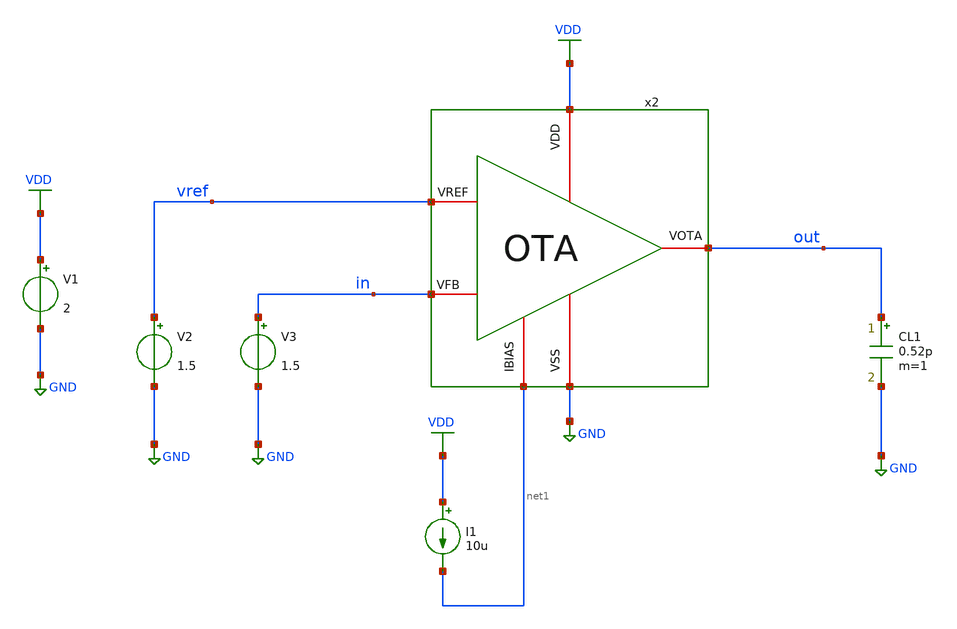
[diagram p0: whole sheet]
** sch_path: designs/libs/tb_ldo/tb_ldo/tb_ldo_OTA/tb_ldo_OTA_noise/tb_ldo_OTA_noise.sch
**.subckt tb_ldo_OTA_noise
V1 VDD GND 2
V2 vref GND 1.5
I1 VDD net1 10u
CL1 out GND 0.52p m=1
V3 in GND 1.5
x2 VDD vref in out net1 GND OTA
**** begin user architecture code



.control
save all

** Set sources
alter @V1[AC] = 1

** Simulation
op
noise v(out) V1 dec 100 1 10G

** Plots
setplot noise1
plot onoise_spectrum
plot inoise_spectrum

** Measurements
let output_noise_at_1MHz = onoise_spectrum[600]
print output_noise_at_1MHz

write tb_ldo_OTA_noise.raw

.endc
* ngspice commands




.include $::180MCU_MODELS/design.ngspice
.lib $::180MCU_MODELS/sm141064.ngspice typical
.lib $::180MCU_MODELS/sm141064.ngspice cap_mim
.lib $::180MCU_MODELS/sm141064.ngspice moscap_typical
.lib $::180MCU_MODELS/sm141064.ngspice mimcap_typical
.lib $::180MCU_MODELS/sm141064.ngspice res_typical
* .lib $::180MCU_MODELS/sm141064.ngspice res_statistical
* ngspice commands

**** end user architecture code
**.ends

* expanding   symbol:  libs/core_ldo/ldo/ldo_OTA/OTA.sym # of pins=6
** sym_path: designs/libs/core_ldo/ldo/OTA.sym
** sch_path: designs/libs/core_ldo/ldo/OTA.sch
.subckt OTA VDD VREF VFB VOTA IBIAS VSS
*.iopin VDD
*.iopin VSS
*.iopin VOTA
*.iopin VREF
*.iopin IBIAS
*.iopin VFB
XM3 net2 net2 VDD VDD pfet_05v0 L=2.00u W=8.00u nf=1 ad='int((nf+1)/2) * W/nf * 0.18u' as='int((nf+2)/2) * W/nf * 0.18u'
+ pd='2*int((nf+1)/2) * (W/nf + 0.18u)' ps='2*int((nf+2)/2) * (W/nf + 0.18u)' nrd='0.18u / W' nrs='0.18u / W'
+ sa=0 sb=0 sd=0 m=1
XM4 net3 net3 VDD VDD pfet_05v0 L=2.00u W=8.00u nf=1 ad='int((nf+1)/2) * W/nf * 0.18u' as='int((nf+2)/2) * W/nf * 0.18u'
+ pd='2*int((nf+1)/2) * (W/nf + 0.18u)' ps='2*int((nf+2)/2) * (W/nf + 0.18u)' nrd='0.18u / W' nrs='0.18u / W'
+ sa=0 sb=0 sd=0 m=1
XM5 net4 net2 VDD VDD pfet_05v0 L=2.00u W=8.00u nf=1 ad='int((nf+1)/2) * W/nf * 0.18u' as='int((nf+2)/2) * W/nf * 0.18u'
+ pd='2*int((nf+1)/2) * (W/nf + 0.18u)' ps='2*int((nf+2)/2) * (W/nf + 0.18u)' nrd='0.18u / W' nrs='0.18u / W'
+ sa=0 sb=0 sd=0 m=1
XM6 VOTA net3 VDD VDD pfet_05v0 L=2.00u W=8.00u nf=1 ad='int((nf+1)/2) * W/nf * 0.18u' as='int((nf+2)/2) * W/nf * 0.18u'
+ pd='2*int((nf+1)/2) * (W/nf + 0.18u)' ps='2*int((nf+2)/2) * (W/nf + 0.18u)' nrd='0.18u / W' nrs='0.18u / W'
+ sa=0 sb=0 sd=0 m=2
XM9 IBIAS IBIAS VSS VSS nfet_05v0 L=2.00u W=4.00u nf=1 ad='int((nf+1)/2) * W/nf * 0.18u' as='int((nf+2)/2) * W/nf * 0.18u'
+ pd='2*int((nf+1)/2) * (W/nf + 0.18u)' ps='2*int((nf+2)/2) * (W/nf + 0.18u)' nrd='0.18u / W' nrs='0.18u / W'
+ sa=0 sb=0 sd=0 m=1
XM10 net1 IBIAS VSS VSS nfet_05v0 L=2.00u W=4.00u nf=1 ad='int((nf+1)/2) * W/nf * 0.18u' as='int((nf+2)/2) * W/nf * 0.18u'
+ pd='2*int((nf+1)/2) * (W/nf + 0.18u)' ps='2*int((nf+2)/2) * (W/nf + 0.18u)' nrd='0.18u / W' nrs='0.18u / W'
+ sa=0 sb=0 sd=0 m=1
XM7 net4 net4 VSS VSS nfet_05v0 L=2.00u W=4.00u nf=1 ad='int((nf+1)/2) * W/nf * 0.18u' as='int((nf+2)/2) * W/nf * 0.18u'
+ pd='2*int((nf+1)/2) * (W/nf + 0.18u)' ps='2*int((nf+2)/2) * (W/nf + 0.18u)' nrd='0.18u / W' nrs='0.18u / W'
+ sa=0 sb=0 sd=0 m=1
XM8 VOTA net4 VSS VSS nfet_05v0 L=2.00u W=4.00u nf=1 ad='int((nf+1)/2) * W/nf * 0.18u' as='int((nf+2)/2) * W/nf * 0.18u'
+ pd='2*int((nf+1)/2) * (W/nf + 0.18u)' ps='2*int((nf+2)/2) * (W/nf + 0.18u)' nrd='0.18u / W' nrs='0.18u / W'
+ sa=0 sb=0 sd=0 m=2
XM1 net2 VREF net1 net1 nfet_05v0 L=0.60u W=40.00u nf=1 ad='int((nf+1)/2) * W/nf * 0.18u' as='int((nf+2)/2) * W/nf * 0.18u'
+ pd='2*int((nf+1)/2) * (W/nf + 0.18u)' ps='2*int((nf+2)/2) * (W/nf + 0.18u)' nrd='0.18u / W' nrs='0.18u / W'
+ sa=0 sb=0 sd=0 m=1
XM2 net3 VFB net1 net1 nfet_05v0 L=0.60u W=40.00u nf=1 ad='int((nf+1)/2) * W/nf * 0.18u' as='int((nf+2)/2) * W/nf * 0.18u'
+ pd='2*int((nf+1)/2) * (W/nf + 0.18u)' ps='2*int((nf+2)/2) * (W/nf + 0.18u)' nrd='0.18u / W' nrs='0.18u / W'
+ sa=0 sb=0 sd=0 m=1
.ends

.GLOBAL GND
.GLOBAL VDD
.end
